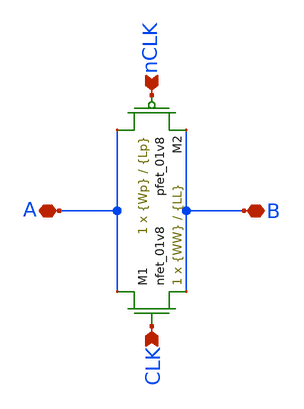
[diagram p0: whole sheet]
** sch_path: schematic/switch.sch
**.subckt switch B A CLK nCLK
*.iopin B
*.iopin A
*.ipin CLK
*.ipin nCLK
XM1 A CLK B GND sky130_fd_pr__nfet_01v8 L={LL} W={WW} nf=1 ad='int((nf+1)/2) * W/nf * 0.29' as='int((nf+2)/2) * W/nf * 0.29'
+ pd='2*int((nf+1)/2) * (W/nf + 0.29)' ps='2*int((nf+2)/2) * (W/nf + 0.29)' nrd='0.29 / W' nrs='0.29 / W'
+ sa=0 sb=0 sd=0 mult=1 m=1
XM2 A nCLK B VDD sky130_fd_pr__pfet_01v8 L={Lp} W={Wp} nf=1 ad='int((nf+1)/2) * W/nf * 0.29' as='int((nf+2)/2) * W/nf * 0.29'
+ pd='2*int((nf+1)/2) * (W/nf + 0.29)' ps='2*int((nf+2)/2) * (W/nf + 0.29)' nrd='0.29 / W' nrs='0.29 / W'
+ sa=0 sb=0 sd=0 mult=1 m=1
**.ends
.end
